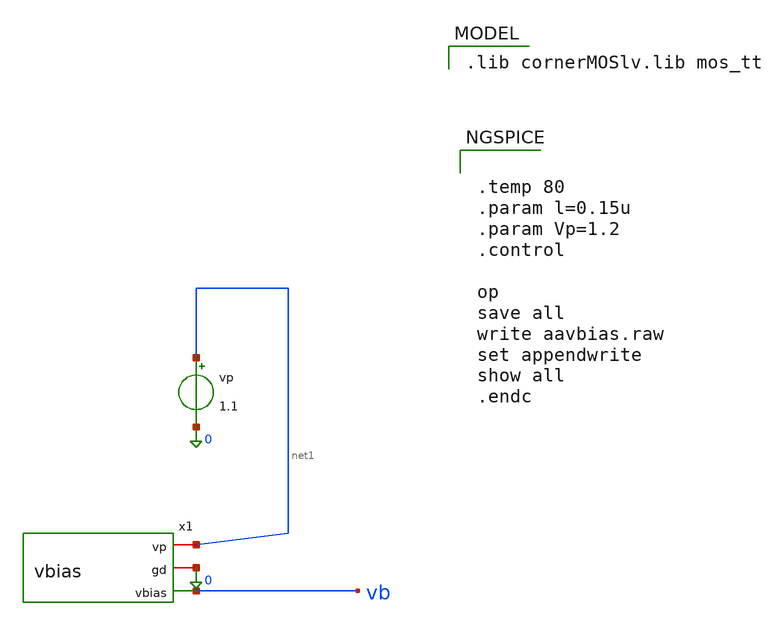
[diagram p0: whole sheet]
** sch_path: charge_pump/vbias_n_tb.sch
**.subckt vbias_n_tb
vp net1 0 1.1
x1 net1 0 vb vbias
**** begin user architecture code
 .lib cornerMOSlv.lib mos_tt



.temp 80
.param l=0.15u
.param Vp=1.2
.control

op
save all
write aavbias.raw
set appendwrite
show all
.endc


**** end user architecture code
**.ends

* expanding   symbol:  /foss/designs/CHIP-PLL/charge_pump/vbias.sym # of pins=3
** sym_path: schematics/charge_pump/vbias.sym
** sch_path: schematics/charge_pump/vbias.sch
.subckt vbias vp gd vbias
*.opin vbias
*.iopin gd
*.iopin vp
XM5 net1 iref vp vp sg13_lv_pmos w=1.2u l=0.6u ng=1 m=1 mm_ok=1
XM6 vbias net1 net2 gd sg13_lv_nmos w=3.6u l=0.6u ng=1 m=1 mm_ok=1
XM2 net2 net2 gd gd sg13_lv_nmos w=1.2u l=0.6u ng=1 m=1 mm_ok=1
XM3 gd gd gd gd sg13_lv_nmos w=1.86u l=0.6u ng=1 m=1 mm_ok=1
XM7 vp vp vp vp sg13_lv_pmos w=1.375u l=0.6u ng=1 m=1 mm_ok=1
XR1 net1 vbias gd rppd w=1e-6 l=1.7e-6 m=1 b=0 mm_ok=1
x1 vp iref gd curr_source
.ends


* expanding   symbol:  /foss/designs/CHIP-PLL/schematics/charge_pump/curr_source.sym # of pins=3
** sym_path: charge_pump/curr_source.sym
** sch_path: charge_pump/curr_source.sch
.subckt curr_source vp iref gd
*.iopin vp
*.iopin gd
*.opin iref
XM4 iref iref vp vp sg13_lv_pmos w=2.2u l=0.15u ng=1 m=1 mm_ok=1
XM5 net1 iref vp vp sg13_lv_pmos w=2.5u l=0.15u ng=1 m=1 mm_ok=1
XM6 iref net1 net2 gd sg13_lv_nmos w=3u l=0.15u ng=1 m=1 mm_ok=1
XM7 net1 net1 gd gd sg13_lv_nmos w=2.2u l=0.15u ng=1 m=1 mm_ok=1
R2 net2 gd 500 m=1
.ends

.end
